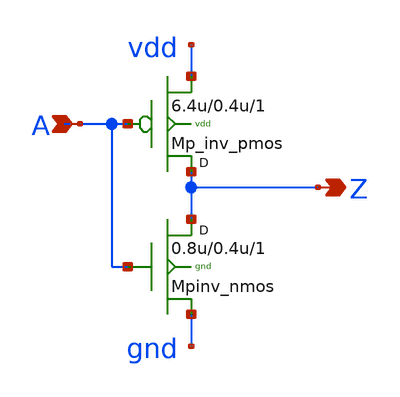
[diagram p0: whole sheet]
** sch_path: sram_2_64_scn4m_lcc/pinv_1.sch
**.subckt pinv_1 A Z
*.ipin A
*.opin Z
Mpinv_nmos Z A gnd gnd n w=0.8u l=0.4u m=1
Mp_inv_pmos Z A vdd vdd p w=6.4u l=0.4u m=1
**.ends
.end
